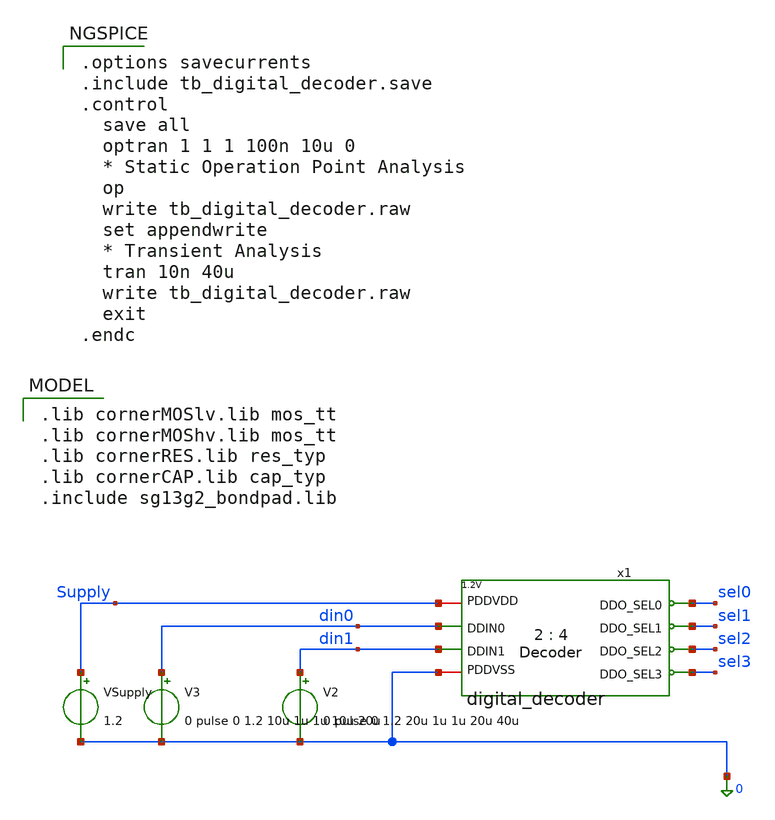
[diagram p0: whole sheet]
** sch_path: xschem/tb_digital_decoder.sch
**.subckt tb_digital_decoder
x1 Supply din1 sel0 din0 sel1 sel2 sel3 0 digital_decoder
VSupply Supply 0 1.2
V2 din1 0 0 pulse 0 1.2 20u 1u 1u 20u 40u
V3 din0 0 0 pulse 0 1.2 10u 1u 1u 10u 20u
**** begin user architecture code

.options savecurrents
.include tb_digital_decoder.save
.control
  save all
  optran 1 1 1 100n 10u 0
  * Static Operation Point Analysis
  op
  write tb_digital_decoder.raw
  set appendwrite
  * Transient Analysis
  tran 10n 40u
  write tb_digital_decoder.raw
  exit
.endc



.lib cornerMOSlv.lib mos_tt
.lib cornerMOShv.lib mos_tt
.lib cornerRES.lib res_typ
.lib cornerCAP.lib cap_typ
.include sg13g2_bondpad.lib


**** end user architecture code
**.ends

* expanding   symbol:  digital_decoder.sym # of pins=8
** sym_path: xschem/digital_decoder.sym
** sch_path: xschem/digital_decoder.sch
.subckt digital_decoder PDDVDD DDIN1 DDO_SEL0 DDIN0 DDO_SEL1 DDO_SEL2 DDO_SEL3 PDDVSS
*.ipin DDIN1
*.ipin DDIN0
*.opin DDO_SEL0
*.iopin PDDVDD
*.iopin PDDVSS
*.opin DDO_SEL1
*.opin DDO_SEL2
*.opin DDO_SEL3
XM1 inv_d1 DDIN1 PDDVDD PDDVDD sg13_lv_pmos w=0.3u l=0.13u ng=1 m=1 mm_ok=1
XM2 inv_d1 DDIN1 PDDVSS PDDVSS sg13_lv_nmos w=0.15u l=0.13u ng=1 m=1 mm_ok=1
XM3 d1 inv_d1 PDDVDD PDDVDD sg13_lv_pmos w=0.3u l=0.13u ng=1 m=1 mm_ok=1
XM4 d1 inv_d1 PDDVSS PDDVSS sg13_lv_nmos w=0.15u l=0.13u ng=1 m=1 mm_ok=1
XM5 inv_d0 DDIN0 PDDVDD PDDVDD sg13_lv_pmos w=0.3u l=0.13u ng=1 m=1 mm_ok=1
XM6 inv_d0 DDIN0 PDDVSS PDDVSS sg13_lv_nmos w=0.15u l=0.13u ng=1 m=1 mm_ok=1
XM7 d0 inv_d0 PDDVDD PDDVDD sg13_lv_pmos w=0.3u l=0.13u ng=1 m=1 mm_ok=1
XM8 d0 inv_d0 PDDVSS PDDVSS sg13_lv_nmos w=0.15u l=0.13u ng=1 m=1 mm_ok=1
XM9 DDO_SEL0 inv_d1 PDDVDD PDDVDD sg13_lv_pmos w=0.3u l=0.13u ng=1 m=1 mm_ok=1
XM10 DDO_SEL0 inv_d1 net2 PDDVSS sg13_lv_nmos w=0.15u l=0.13u ng=1 m=1 mm_ok=1
XM11 DDO_SEL1 inv_d1 PDDVDD PDDVDD sg13_lv_pmos w=0.3u l=0.13u ng=1 m=1 mm_ok=1
XM12 DDO_SEL1 inv_d1 net3 PDDVSS sg13_lv_nmos w=0.15u l=0.13u ng=1 m=1 mm_ok=1
XM13 DDO_SEL2 inv_d0 PDDVDD PDDVDD sg13_lv_pmos w=0.3u l=0.13u ng=1 m=1 mm_ok=1
XM14 DDO_SEL2 inv_d0 net4 PDDVSS sg13_lv_nmos w=0.15u l=0.13u ng=1 m=1 mm_ok=1
XM15 DDO_SEL3 d1 PDDVDD PDDVDD sg13_lv_pmos w=0.3u l=0.13u ng=1 m=1 mm_ok=1
XM16 DDO_SEL3 d1 net1 PDDVSS sg13_lv_nmos w=0.15u l=0.13u ng=1 m=1 mm_ok=1
XM19 DDO_SEL0 inv_d0 PDDVDD PDDVDD sg13_lv_pmos w=0.3u l=0.13u ng=1 m=1 mm_ok=1
XM20 DDO_SEL1 d0 PDDVDD PDDVDD sg13_lv_pmos w=0.3u l=0.13u ng=1 m=1 mm_ok=1
XM21 DDO_SEL2 d1 PDDVDD PDDVDD sg13_lv_pmos w=0.3u l=0.13u ng=1 m=1 mm_ok=1
XM22 DDO_SEL3 d0 PDDVDD PDDVDD sg13_lv_pmos w=0.3u l=0.13u ng=1 m=1 mm_ok=1
XM23 net2 inv_d0 PDDVSS PDDVSS sg13_lv_nmos w=0.15u l=0.13u ng=1 m=1 mm_ok=1
XM24 net3 d0 PDDVSS PDDVSS sg13_lv_nmos w=0.15u l=0.13u ng=1 m=1 mm_ok=1
XM25 net4 d1 PDDVSS PDDVSS sg13_lv_nmos w=0.15u l=0.13u ng=1 m=1 mm_ok=1
XM26 net1 d0 PDDVSS PDDVSS sg13_lv_nmos w=0.15u l=0.13u ng=1 m=1 mm_ok=1
.ends

.end
